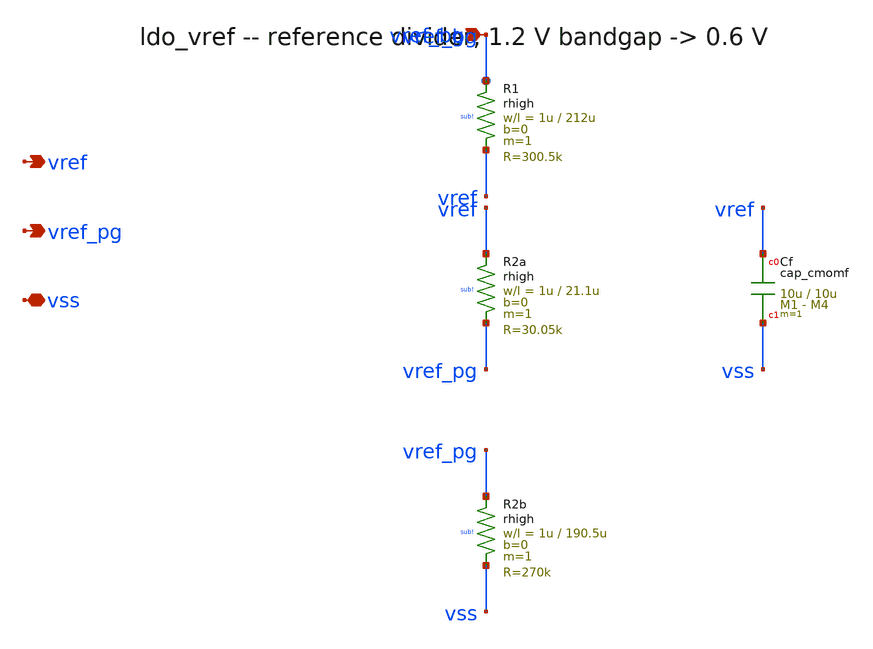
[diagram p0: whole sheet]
** sch_path: xschem/ldo_vref.sch
**.subckt ldo_vref vref_bg vref vref_pg vss
*.ipin vref_bg
*.opin vref
*.opin vref_pg
*.iopin vss
XR1 vref_bg vref sub! rhigh w=1u l=212u m=1 b=0 mm_ok=1
XR2a vref vref_pg sub! rhigh w=1u l=21.1u m=1 b=0 mm_ok=1
XR2b vref_pg vss sub! rhigh w=1u l=190.5u m=1 b=0 mm_ok=1
XCf vref vss cap_cmomf w=10u l=10u mmin=1 mmax=4 subblock=0 rfmodel=0 subscale=1 m=1 mm_ok=1
**.ends
.end
